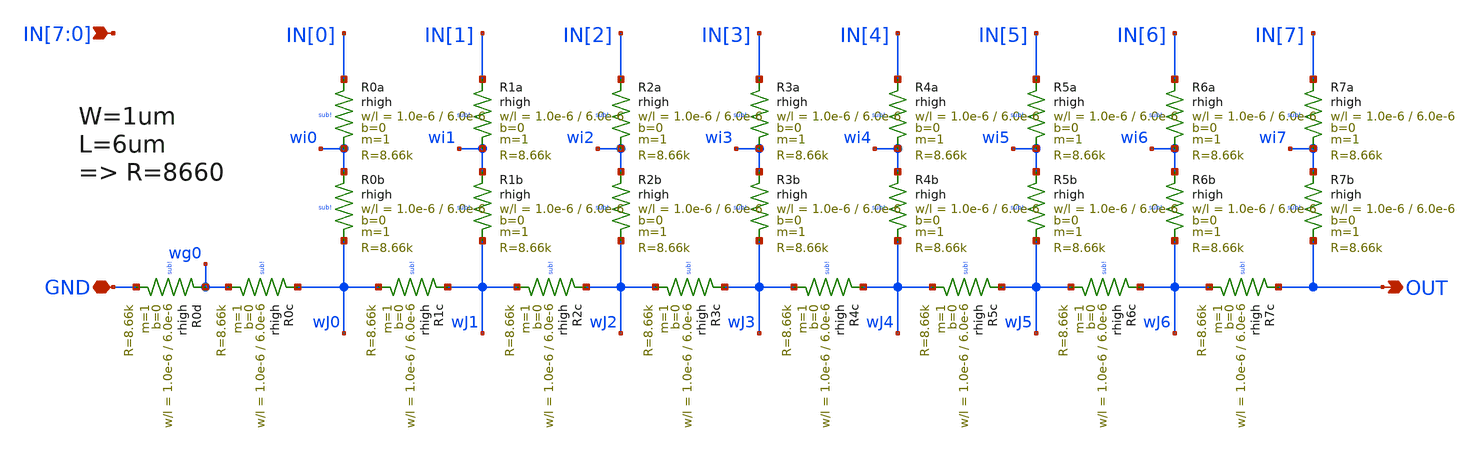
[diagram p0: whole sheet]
** sch_path: xschem/r2r_dac.sch
**.subckt r2r_dac IN[7],IN[6],IN[5],IN[4],IN[3],IN[2],IN[1],IN[0] GND OUT
*.ipin IN[7],IN[6],IN[5],IN[4],IN[3],IN[2],IN[1],IN[0]
*.iopin GND
*.opin OUT
XR0a IN[0] wi0 sub! rhigh w=1.0e-6 l=6.0e-6 m=1 b=0 mm_ok=1
XR0b wi0 wJ0 sub! rhigh w=1.0e-6 l=6.0e-6 m=1 b=0 mm_ok=1
XR1c wJ1 wJ0 sub! rhigh w=1.0e-6 l=6.0e-6 m=1 b=0 mm_ok=1
XR0c wJ0 wg0 sub! rhigh w=1.0e-6 l=6.0e-6 m=1 b=0 mm_ok=1
XR0d wg0 GND sub! rhigh w=1.0e-6 l=6.0e-6 m=1 b=0 mm_ok=1
XR1a IN[1] wi1 sub! rhigh w=1.0e-6 l=6.0e-6 m=1 b=0 mm_ok=1
XR1b wi1 wJ1 sub! rhigh w=1.0e-6 l=6.0e-6 m=1 b=0 mm_ok=1
XR2c wJ2 wJ1 sub! rhigh w=1.0e-6 l=6.0e-6 m=1 b=0 mm_ok=1
XR2a IN[2] wi2 sub! rhigh w=1.0e-6 l=6.0e-6 m=1 b=0 mm_ok=1
XR2b wi2 wJ2 sub! rhigh w=1.0e-6 l=6.0e-6 m=1 b=0 mm_ok=1
XR3c wJ3 wJ2 sub! rhigh w=1.0e-6 l=6.0e-6 m=1 b=0 mm_ok=1
XR3a IN[3] wi3 sub! rhigh w=1.0e-6 l=6.0e-6 m=1 b=0 mm_ok=1
XR3b wi3 wJ3 sub! rhigh w=1.0e-6 l=6.0e-6 m=1 b=0 mm_ok=1
XR4c wJ4 wJ3 sub! rhigh w=1.0e-6 l=6.0e-6 m=1 b=0 mm_ok=1
XR4a IN[4] wi4 sub! rhigh w=1.0e-6 l=6.0e-6 m=1 b=0 mm_ok=1
XR4b wi4 wJ4 sub! rhigh w=1.0e-6 l=6.0e-6 m=1 b=0 mm_ok=1
XR5c wJ5 wJ4 sub! rhigh w=1.0e-6 l=6.0e-6 m=1 b=0 mm_ok=1
XR5a IN[5] wi5 sub! rhigh w=1.0e-6 l=6.0e-6 m=1 b=0 mm_ok=1
XR5b wi5 wJ5 sub! rhigh w=1.0e-6 l=6.0e-6 m=1 b=0 mm_ok=1
XR6c wJ6 wJ5 sub! rhigh w=1.0e-6 l=6.0e-6 m=1 b=0 mm_ok=1
XR6a IN[6] wi6 sub! rhigh w=1.0e-6 l=6.0e-6 m=1 b=0 mm_ok=1
XR6b wi6 wJ6 sub! rhigh w=1.0e-6 l=6.0e-6 m=1 b=0 mm_ok=1
XR7c OUT wJ6 sub! rhigh w=1.0e-6 l=6.0e-6 m=1 b=0 mm_ok=1
XR7a IN[7] wi7 sub! rhigh w=1.0e-6 l=6.0e-6 m=1 b=0 mm_ok=1
XR7b wi7 OUT sub! rhigh w=1.0e-6 l=6.0e-6 m=1 b=0 mm_ok=1
**.ends
.end
